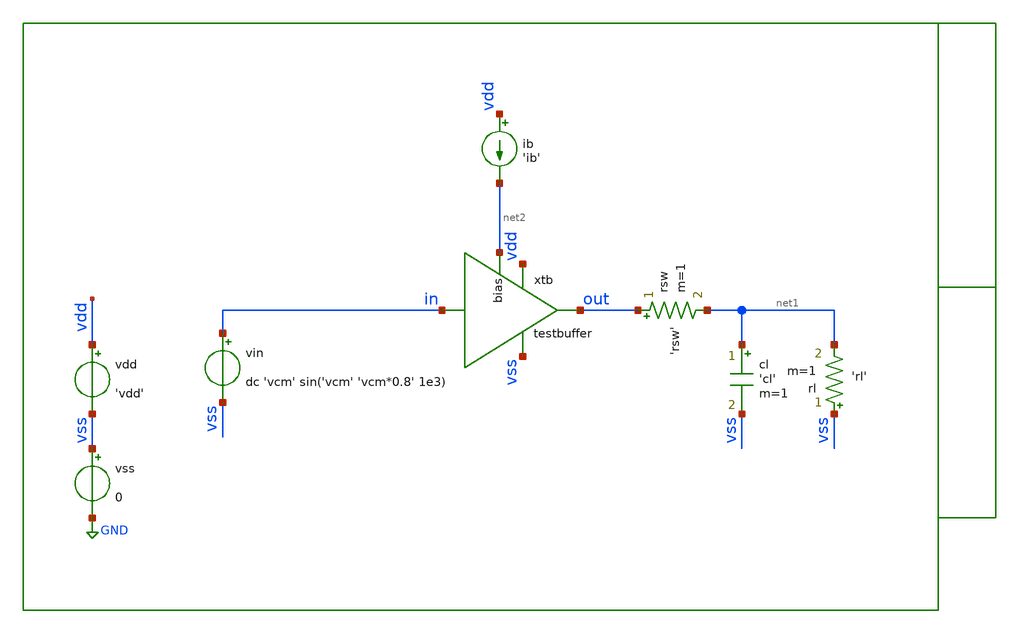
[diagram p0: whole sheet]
** sch_path: xschem/tb/testbuffer/testbuffer/tr_testbuffer.sch
**.subckt tr_testbuffer
vin in vss dc 'vcm' sin('vcm' 'vcm*0.8' 1e3)
ib vdd net2 'ib'
cl net1 vss 'cl' m=1
rl vss net1 'rl' m=1
vdd vdd vss 'vdd'
vss vss GND 0
rsw out net1 'rsw' m=1
xtb vdd out in vss net2 testbuffer
**** begin user architecture code
 * Control

.param vdd=3.3
.param vcm='vdd/2'
.param ib=5u
.param cl=10p
.param rl=1e6
.param rsw=20

.control
set wr_singlescale
set wr_vecnames
set filetype=ascii
*set interp

save all
tran 1u 1m
gnuplot p1 in out
*tran 1u 1000m
*wrdata output.csv out
.endc

 * Model Corners

.include $::CORNERS/ngspice/tt.spice
*.include $::CORNERS/ngspice/ff.spice
*.include $::CORNERS/ngspice/ss.spice
*.include $::CORNERS/ngspice/sf.spice
*.include $::CORNERS/ngspice/fs.spice

**** end user architecture code
**.ends

* expanding   symbol:  sch/testbuffer/testbuffer/testbuffer.sym # of pins=5
** sym_path: xschem/sch/testbuffer/testbuffer/testbuffer.sym
** sch_path: xschem/sch/testbuffer/testbuffer/testbuffer.sch
.subckt testbuffer vdd out in vss bias
*.ipin in
*.opin out
*.iopin vdd
*.iopin vss
*.iopin bias
xamp vdd out in out vss bias tb_amplifier
.ends


* expanding   symbol:  sch/testbuffer/tb_amplifier/tb_amplifier.sym # of pins=6
** sym_path: xschem/sch/testbuffer/tb_amplifier/tb_amplifier.sym
** sch_path: xschem/sch/testbuffer/tb_amplifier/tb_amplifier.sch
.subckt tb_amplifier vdd out inp inn vss bias
*.ipin inn
*.ipin inp
*.opin out
*.iopin bias
*.iopin vdd
*.iopin vss
XM3 mirr mirr vdd vdd pfet_06v0 L=4u W=16u nf=2 ad='int((nf+1)/2) * W/nf * 0.18u' as='int((nf+2)/2) * W/nf * 0.18u'
+ pd='2*int((nf+1)/2) * (W/nf + 0.18u)' ps='2*int((nf+2)/2) * (W/nf + 0.18u)' nrd='0.18u / W' nrs='0.18u / W'
+ sa=0 sb=0 sd=0 m=2 par=2
XM4 comp mirr vdd vdd pfet_06v0 L=4u W=16u nf=2 ad='int((nf+1)/2) * W/nf * 0.18u' as='int((nf+2)/2) * W/nf * 0.18u'
+ pd='2*int((nf+1)/2) * (W/nf + 0.18u)' ps='2*int((nf+2)/2) * (W/nf + 0.18u)' nrd='0.18u / W' nrs='0.18u / W'
+ sa=0 sb=0 sd=0 m=2 par=2
XM2 comp inp vcm vss nfet_06v0 L=2u W=16u nf=2 ad='int((nf+1)/2) * W/nf * 0.18u' as='int((nf+2)/2) * W/nf * 0.18u'
+ pd='2*int((nf+1)/2) * (W/nf + 0.18u)' ps='2*int((nf+2)/2) * (W/nf + 0.18u)' nrd='0.18u / W' nrs='0.18u / W'
+ sa=0 sb=0 sd=0 m=2 par=2
XM1 mirr inn vcm vss nfet_06v0 L=2u W=16u nf=2 ad='int((nf+1)/2) * W/nf * 0.18u' as='int((nf+2)/2) * W/nf * 0.18u'
+ pd='2*int((nf+1)/2) * (W/nf + 0.18u)' ps='2*int((nf+2)/2) * (W/nf + 0.18u)' nrd='0.18u / W' nrs='0.18u / W'
+ sa=0 sb=0 sd=0 m=2 par=2
XM5 vcm bias vss vss nfet_06v0 L=1u W=16u nf=2 ad='int((nf+1)/2) * W/nf * 0.18u' as='int((nf+2)/2) * W/nf * 0.18u'
+ pd='2*int((nf+1)/2) * (W/nf + 0.18u)' ps='2*int((nf+2)/2) * (W/nf + 0.18u)' nrd='0.18u / W' nrs='0.18u / W'
+ sa=0 sb=0 sd=0 m=2 par=2
XM6 out bias vss vss nfet_06v0 L=1u W=16u nf=2 ad='int((nf+1)/2) * W/nf * 0.18u' as='int((nf+2)/2) * W/nf * 0.18u'
+ pd='2*int((nf+1)/2) * (W/nf + 0.18u)' ps='2*int((nf+2)/2) * (W/nf + 0.18u)' nrd='0.18u / W' nrs='0.18u / W'
+ sa=0 sb=0 sd=0 m=12 par=12
XM7 out comp vdd vdd pfet_06v0 L=1u W=96u nf=12 ad='int((nf+1)/2) * W/nf * 0.18u' as='int((nf+2)/2) * W/nf * 0.18u'
+ pd='2*int((nf+1)/2) * (W/nf + 0.18u)' ps='2*int((nf+2)/2) * (W/nf + 0.18u)' nrd='0.18u / W' nrs='0.18u / W'
+ sa=0 sb=0 sd=0 m=1 par=1
XMB1 bias bias vss vss nfet_06v0 L=1u W=16u nf=2 ad='int((nf+1)/2) * W/nf * 0.18u' as='int((nf+2)/2) * W/nf * 0.18u'
+ pd='2*int((nf+1)/2) * (W/nf + 0.18u)' ps='2*int((nf+2)/2) * (W/nf + 0.18u)' nrd='0.18u / W' nrs='0.18u / W'
+ sa=0 sb=0 sd=0 m=2 par=2
XMB2 vbm bias vss vss nfet_06v0 L=1u W=16u nf=2 ad='int((nf+1)/2) * W/nf * 0.18u' as='int((nf+2)/2) * W/nf * 0.18u'
+ pd='2*int((nf+1)/2) * (W/nf + 0.18u)' ps='2*int((nf+2)/2) * (W/nf + 0.18u)' nrd='0.18u / W' nrs='0.18u / W'
+ sa=0 sb=0 sd=0 m=2 par=2
XMB3 vbm vbm vbt vdd pfet_06v0 L=1u W=16u nf=2 ad='int((nf+1)/2) * W/nf * 0.18u' as='int((nf+2)/2) * W/nf * 0.18u'
+ pd='2*int((nf+1)/2) * (W/nf + 0.18u)' ps='2*int((nf+2)/2) * (W/nf + 0.18u)' nrd='0.18u / W' nrs='0.18u / W'
+ sa=0 sb=0 sd=0 m=1 par=1
XMB4 vbt vbt vdd vdd pfet_06v0 L=1u W=16u nf=2 ad='int((nf+1)/2) * W/nf * 0.18u' as='int((nf+2)/2) * W/nf * 0.18u'
+ pd='2*int((nf+1)/2) * (W/nf + 0.18u)' ps='2*int((nf+2)/2) * (W/nf + 0.18u)' nrd='0.18u / W' nrs='0.18u / W'
+ sa=0 sb=0 sd=0 m=1 par=1
XRCC gc comp vdd ppolyf_u_1k_6p0 r_width=2e-6 r_length=38e-6 s=1 m=1
XMDUM1 vss vss vss vss nfet_06v0 L=2u W=16u nf=2 ad='int((nf+1)/2) * W/nf * 0.18u' as='int((nf+2)/2) * W/nf * 0.18u'
+ pd='2*int((nf+1)/2) * (W/nf + 0.18u)' ps='2*int((nf+2)/2) * (W/nf + 0.18u)' nrd='0.18u / W' nrs='0.18u / W'
+ sa=0 sb=0 sd=0 m=2 par=2
XMDUM2 vdd vdd vdd vdd pfet_06v0 L=4u W=16u nf=2 ad='int((nf+1)/2) * W/nf * 0.18u' as='int((nf+2)/2) * W/nf * 0.18u'
+ pd='2*int((nf+1)/2) * (W/nf + 0.18u)' ps='2*int((nf+2)/2) * (W/nf + 0.18u)' nrd='0.18u / W' nrs='0.18u / W'
+ sa=0 sb=0 sd=0 m=4 par=4
XC1 out gc cap_mim_2f0_m4m5_noshield c_width=30e-6 c_length=30e-6 m=1
.ends

.GLOBAL GND
.end
